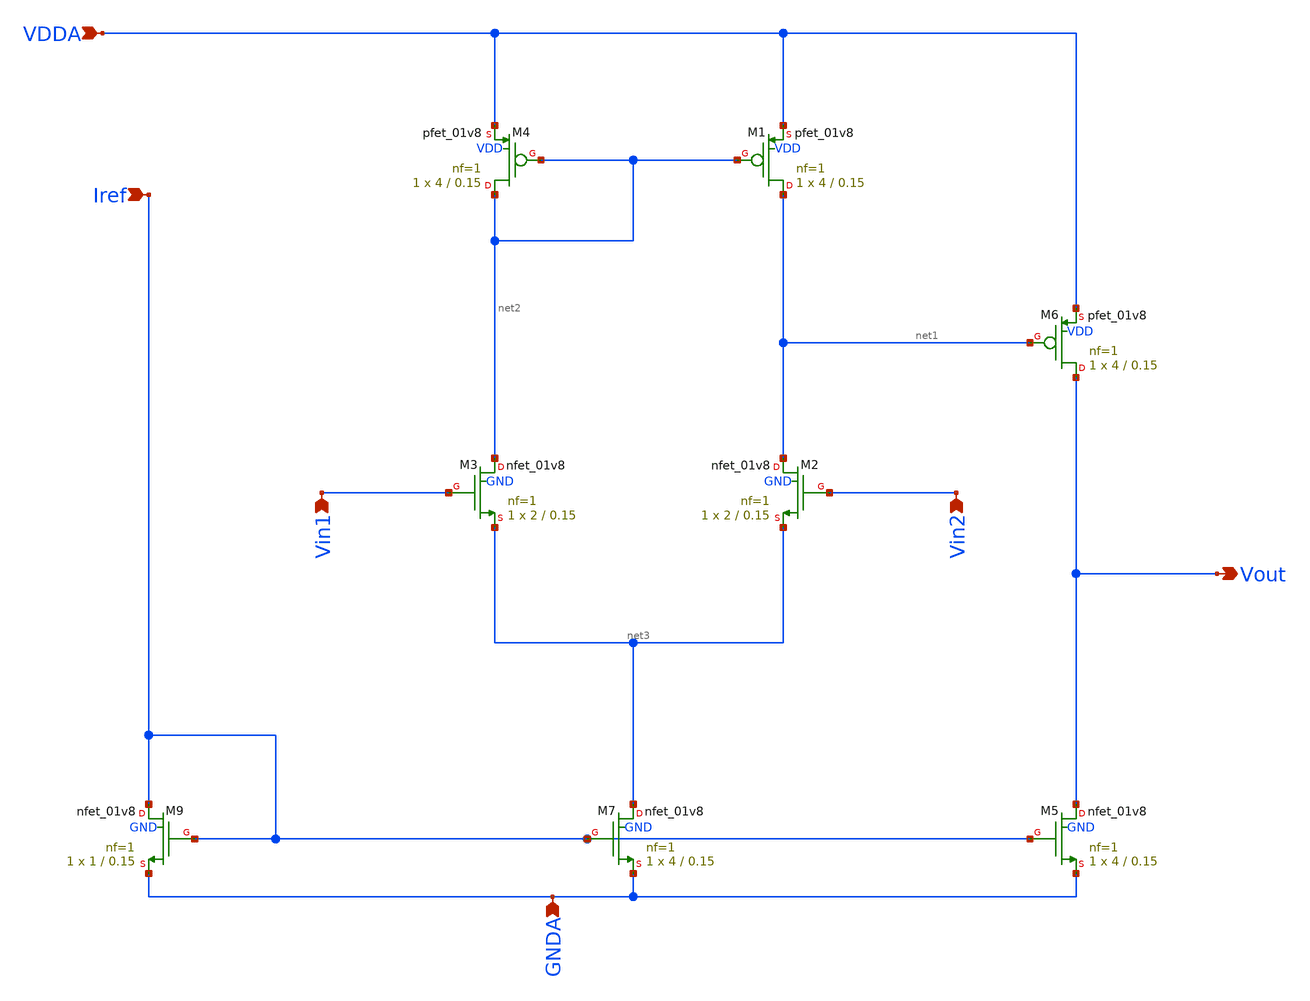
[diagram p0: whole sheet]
** sch_path: projects/pll/trials/opamp22.sch
**.subckt opamp22 Iref Vout Vin2 Vin1 VDDA GNDA
*.ipin Iref
*.opin Vout
*.ipin Vin2
*.ipin Vin1
*.ipin VDDA
*.ipin GNDA
XM1 net1 net2 VDDA VDD sky130_fd_pr__pfet_01v8 L=0.15 W=4 nf=1 ad='int((nf+1)/2) * W/nf * 0.29' as='int((nf+2)/2) * W/nf * 0.29'
+ pd='2*int((nf+1)/2) * (W/nf + 0.29)' ps='2*int((nf+2)/2) * (W/nf + 0.29)' nrd='0.29 / W' nrs='0.29 / W'
+ sa=0 sb=0 sd=0 mult=1 m=1
XM2 net1 Vin2 net3 GND sky130_fd_pr__nfet_01v8 L=0.15 W=2 nf=1 ad='int((nf+1)/2) * W/nf * 0.29' as='int((nf+2)/2) * W/nf * 0.29'
+ pd='2*int((nf+1)/2) * (W/nf + 0.29)' ps='2*int((nf+2)/2) * (W/nf + 0.29)' nrd='0.29 / W' nrs='0.29 / W'
+ sa=0 sb=0 sd=0 mult=1 m=1
XM3 net2 Vin1 net3 GND sky130_fd_pr__nfet_01v8 L=0.15 W=2 nf=1 ad='int((nf+1)/2) * W/nf * 0.29' as='int((nf+2)/2) * W/nf * 0.29'
+ pd='2*int((nf+1)/2) * (W/nf + 0.29)' ps='2*int((nf+2)/2) * (W/nf + 0.29)' nrd='0.29 / W' nrs='0.29 / W'
+ sa=0 sb=0 sd=0 mult=1 m=1
XM4 net2 net2 VDDA VDD sky130_fd_pr__pfet_01v8 L=0.15 W=4 nf=1 ad='int((nf+1)/2) * W/nf * 0.29' as='int((nf+2)/2) * W/nf * 0.29'
+ pd='2*int((nf+1)/2) * (W/nf + 0.29)' ps='2*int((nf+2)/2) * (W/nf + 0.29)' nrd='0.29 / W' nrs='0.29 / W'
+ sa=0 sb=0 sd=0 mult=1 m=1
XM5 Vout Iref GNDA GND sky130_fd_pr__nfet_01v8 L=0.15 W=4 nf=1 ad='int((nf+1)/2) * W/nf * 0.29' as='int((nf+2)/2) * W/nf * 0.29'
+ pd='2*int((nf+1)/2) * (W/nf + 0.29)' ps='2*int((nf+2)/2) * (W/nf + 0.29)' nrd='0.29 / W' nrs='0.29 / W'
+ sa=0 sb=0 sd=0 mult=1 m=1
XM6 Vout net1 VDDA VDD sky130_fd_pr__pfet_01v8 L=0.15 W=4 nf=1 ad='int((nf+1)/2) * W/nf * 0.29' as='int((nf+2)/2) * W/nf * 0.29'
+ pd='2*int((nf+1)/2) * (W/nf + 0.29)' ps='2*int((nf+2)/2) * (W/nf + 0.29)' nrd='0.29 / W' nrs='0.29 / W'
+ sa=0 sb=0 sd=0 mult=1 m=1
XM7 net3 Iref GNDA GND sky130_fd_pr__nfet_01v8 L=0.15 W=4 nf=1 ad='int((nf+1)/2) * W/nf * 0.29' as='int((nf+2)/2) * W/nf * 0.29'
+ pd='2*int((nf+1)/2) * (W/nf + 0.29)' ps='2*int((nf+2)/2) * (W/nf + 0.29)' nrd='0.29 / W' nrs='0.29 / W'
+ sa=0 sb=0 sd=0 mult=1 m=1
XM9 Iref Iref GNDA GND sky130_fd_pr__nfet_01v8 L=0.15 W=1 nf=1 ad='int((nf+1)/2) * W/nf * 0.29' as='int((nf+2)/2) * W/nf * 0.29'
+ pd='2*int((nf+1)/2) * (W/nf + 0.29)' ps='2*int((nf+2)/2) * (W/nf + 0.29)' nrd='0.29 / W' nrs='0.29 / W'
+ sa=0 sb=0 sd=0 mult=1 m=1
**.ends
.end
